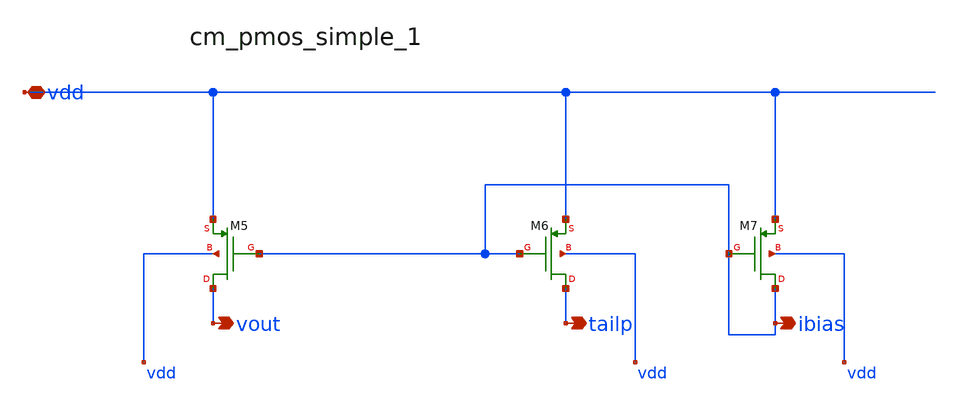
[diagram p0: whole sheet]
** sch_path: analog-db/raw/amp_024_smcnr/hier/blocks/cm_pmos_simple_1.sch
**.subckt cm_pmos_simple_1 vdd ibias vout tailp
*.iopin vdd
*.opin ibias
*.opin vout
*.opin tailp
XM5 vout ibias vdd vdd sg13_lv_pmos w=x_dut_xm5_w l=x_dut_xm5_l ng=1 m=x_dut_xm5_m
XM6 tailp ibias vdd vdd sg13_lv_pmos w=x_dut_xm6_w l=x_dut_xm6_l ng=1 m=x_dut_xm6_m
XM7 ibias ibias vdd vdd sg13_lv_pmos w=x_dut_xm7_w l=x_dut_xm7_l ng=1 m=x_dut_xm7_m
**.ends
.end
